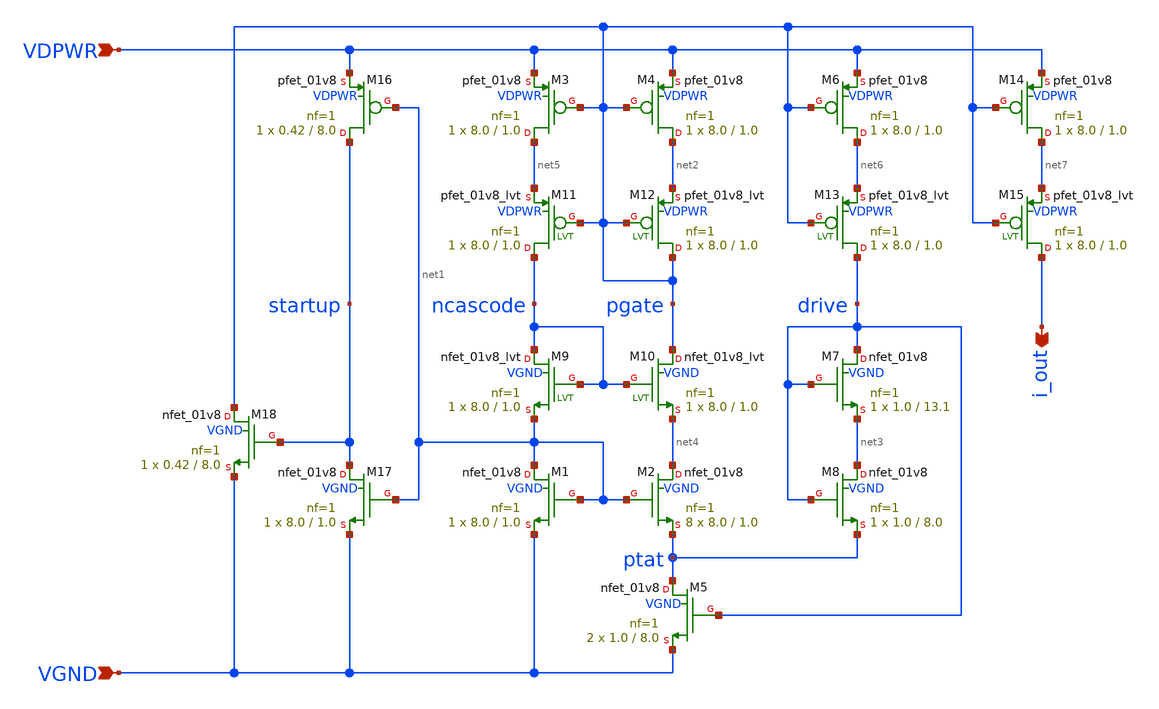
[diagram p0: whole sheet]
** sch_path: xschem/bias_generator.sch
**.subckt bias_generator VGND VDPWR i_out
*.ipin VGND
*.ipin VDPWR
*.opin i_out
XM9 ncascode ncascode net1 VGND sky130_fd_pr__nfet_01v8_lvt L=1.0 W=8.0 nf=1 ad='int((nf+1)/2) * W/nf * 0.29'
+ as='int((nf+2)/2) * W/nf * 0.29' pd='2*int((nf+1)/2) * (W/nf + 0.29)' ps='2*int((nf+2)/2) * (W/nf + 0.29)'
+ nrd='0.29 / W' nrs='0.29 / W' sa=0 sb=0 sd=0 mult=1 m=1
XM10 pgate ncascode net4 VGND sky130_fd_pr__nfet_01v8_lvt L=1.0 W=8.0 nf=1 ad='int((nf+1)/2) * W/nf * 0.29'
+ as='int((nf+2)/2) * W/nf * 0.29' pd='2*int((nf+1)/2) * (W/nf + 0.29)' ps='2*int((nf+2)/2) * (W/nf + 0.29)'
+ nrd='0.29 / W' nrs='0.29 / W' sa=0 sb=0 sd=0 mult=1 m=1
XM2 net4 net1 ptat VGND sky130_fd_pr__nfet_01v8 L=1.0 W=8.0 nf=1 ad='int((nf+1)/2) * W/nf * 0.29' as='int((nf+2)/2) * W/nf * 0.29'
+ pd='2*int((nf+1)/2) * (W/nf + 0.29)' ps='2*int((nf+2)/2) * (W/nf + 0.29)' nrd='0.29 / W' nrs='0.29 / W'
+ sa=0 sb=0 sd=0 mult=8 m=8
XM18 pgate startup VGND VGND sky130_fd_pr__nfet_01v8 L=8.0 W=0.42 nf=1 ad='int((nf+1)/2) * W/nf * 0.29'
+ as='int((nf+2)/2) * W/nf * 0.29' pd='2*int((nf+1)/2) * (W/nf + 0.29)' ps='2*int((nf+2)/2) * (W/nf + 0.29)'
+ nrd='0.29 / W' nrs='0.29 / W' sa=0 sb=0 sd=0 mult=1 m=1
XM17 startup net1 VGND VGND sky130_fd_pr__nfet_01v8 L=1.0 W=8.0 nf=1 ad='int((nf+1)/2) * W/nf * 0.29'
+ as='int((nf+2)/2) * W/nf * 0.29' pd='2*int((nf+1)/2) * (W/nf + 0.29)' ps='2*int((nf+2)/2) * (W/nf + 0.29)'
+ nrd='0.29 / W' nrs='0.29 / W' sa=0 sb=0 sd=0 mult=1 m=1
XM1 net1 net1 VGND VGND sky130_fd_pr__nfet_01v8 L=1.0 W=8.0 nf=1 ad='int((nf+1)/2) * W/nf * 0.29' as='int((nf+2)/2) * W/nf * 0.29'
+ pd='2*int((nf+1)/2) * (W/nf + 0.29)' ps='2*int((nf+2)/2) * (W/nf + 0.29)' nrd='0.29 / W' nrs='0.29 / W'
+ sa=0 sb=0 sd=0 mult=1 m=1
XM5 ptat drive VGND VGND sky130_fd_pr__nfet_01v8 L=8.0 W=1.0 nf=1 ad='int((nf+1)/2) * W/nf * 0.29' as='int((nf+2)/2) * W/nf * 0.29'
+ pd='2*int((nf+1)/2) * (W/nf + 0.29)' ps='2*int((nf+2)/2) * (W/nf + 0.29)' nrd='0.29 / W' nrs='0.29 / W'
+ sa=0 sb=0 sd=0 mult=2 m=2
XM7 drive drive net3 VGND sky130_fd_pr__nfet_01v8 L=13.1 W=1.0 nf=1 ad='int((nf+1)/2) * W/nf * 0.29'
+ as='int((nf+2)/2) * W/nf * 0.29' pd='2*int((nf+1)/2) * (W/nf + 0.29)' ps='2*int((nf+2)/2) * (W/nf + 0.29)'
+ nrd='0.29 / W' nrs='0.29 / W' sa=0 sb=0 sd=0 mult=1 m=1
XM8 net3 drive ptat VGND sky130_fd_pr__nfet_01v8 L=8.0 W=1.0 nf=1 ad='int((nf+1)/2) * W/nf * 0.29' as='int((nf+2)/2) * W/nf * 0.29'
+ pd='2*int((nf+1)/2) * (W/nf + 0.29)' ps='2*int((nf+2)/2) * (W/nf + 0.29)' nrd='0.29 / W' nrs='0.29 / W'
+ sa=0 sb=0 sd=0 mult=1 m=1
XM4 net2 pgate VDPWR VDPWR sky130_fd_pr__pfet_01v8 L=1.0 W=8.0 nf=1 ad='int((nf+1)/2) * W/nf * 0.29'
+ as='int((nf+2)/2) * W/nf * 0.29' pd='2*int((nf+1)/2) * (W/nf + 0.29)' ps='2*int((nf+2)/2) * (W/nf + 0.29)'
+ nrd='0.29 / W' nrs='0.29 / W' sa=0 sb=0 sd=0 mult=1 m=1
XM6 net6 pgate VDPWR VDPWR sky130_fd_pr__pfet_01v8 L=1.0 W=8.0 nf=1 ad='int((nf+1)/2) * W/nf * 0.29'
+ as='int((nf+2)/2) * W/nf * 0.29' pd='2*int((nf+1)/2) * (W/nf + 0.29)' ps='2*int((nf+2)/2) * (W/nf + 0.29)'
+ nrd='0.29 / W' nrs='0.29 / W' sa=0 sb=0 sd=0 mult=1 m=1
XM14 net7 pgate VDPWR VDPWR sky130_fd_pr__pfet_01v8 L=1.0 W=8.0 nf=1 ad='int((nf+1)/2) * W/nf * 0.29'
+ as='int((nf+2)/2) * W/nf * 0.29' pd='2*int((nf+1)/2) * (W/nf + 0.29)' ps='2*int((nf+2)/2) * (W/nf + 0.29)'
+ nrd='0.29 / W' nrs='0.29 / W' sa=0 sb=0 sd=0 mult=1 m=1
XM3 net5 pgate VDPWR VDPWR sky130_fd_pr__pfet_01v8 L=1.0 W=8.0 nf=1 ad='int((nf+1)/2) * W/nf * 0.29'
+ as='int((nf+2)/2) * W/nf * 0.29' pd='2*int((nf+1)/2) * (W/nf + 0.29)' ps='2*int((nf+2)/2) * (W/nf + 0.29)'
+ nrd='0.29 / W' nrs='0.29 / W' sa=0 sb=0 sd=0 mult=1 m=1
XM16 startup net1 VDPWR VDPWR sky130_fd_pr__pfet_01v8 L=8.0 W=0.42 nf=1 ad='int((nf+1)/2) * W/nf * 0.29'
+ as='int((nf+2)/2) * W/nf * 0.29' pd='2*int((nf+1)/2) * (W/nf + 0.29)' ps='2*int((nf+2)/2) * (W/nf + 0.29)'
+ nrd='0.29 / W' nrs='0.29 / W' sa=0 sb=0 sd=0 mult=1 m=1
XM12 pgate pgate net2 VDPWR sky130_fd_pr__pfet_01v8_lvt L=1.0 W=8.0 nf=1 ad='int((nf+1)/2) * W/nf * 0.29'
+ as='int((nf+2)/2) * W/nf * 0.29' pd='2*int((nf+1)/2) * (W/nf + 0.29)' ps='2*int((nf+2)/2) * (W/nf + 0.29)'
+ nrd='0.29 / W' nrs='0.29 / W' sa=0 sb=0 sd=0 mult=1 m=1
XM13 drive pgate net6 VDPWR sky130_fd_pr__pfet_01v8_lvt L=1.0 W=8.0 nf=1 ad='int((nf+1)/2) * W/nf * 0.29'
+ as='int((nf+2)/2) * W/nf * 0.29' pd='2*int((nf+1)/2) * (W/nf + 0.29)' ps='2*int((nf+2)/2) * (W/nf + 0.29)'
+ nrd='0.29 / W' nrs='0.29 / W' sa=0 sb=0 sd=0 mult=1 m=1
XM15 i_out pgate net7 VDPWR sky130_fd_pr__pfet_01v8_lvt L=1.0 W=8.0 nf=1 ad='int((nf+1)/2) * W/nf * 0.29'
+ as='int((nf+2)/2) * W/nf * 0.29' pd='2*int((nf+1)/2) * (W/nf + 0.29)' ps='2*int((nf+2)/2) * (W/nf + 0.29)'
+ nrd='0.29 / W' nrs='0.29 / W' sa=0 sb=0 sd=0 mult=1 m=1
XM11 ncascode pgate net5 VDPWR sky130_fd_pr__pfet_01v8_lvt L=1.0 W=8.0 nf=1 ad='int((nf+1)/2) * W/nf * 0.29'
+ as='int((nf+2)/2) * W/nf * 0.29' pd='2*int((nf+1)/2) * (W/nf + 0.29)' ps='2*int((nf+2)/2) * (W/nf + 0.29)'
+ nrd='0.29 / W' nrs='0.29 / W' sa=0 sb=0 sd=0 mult=1 m=1
**.ends
.end
